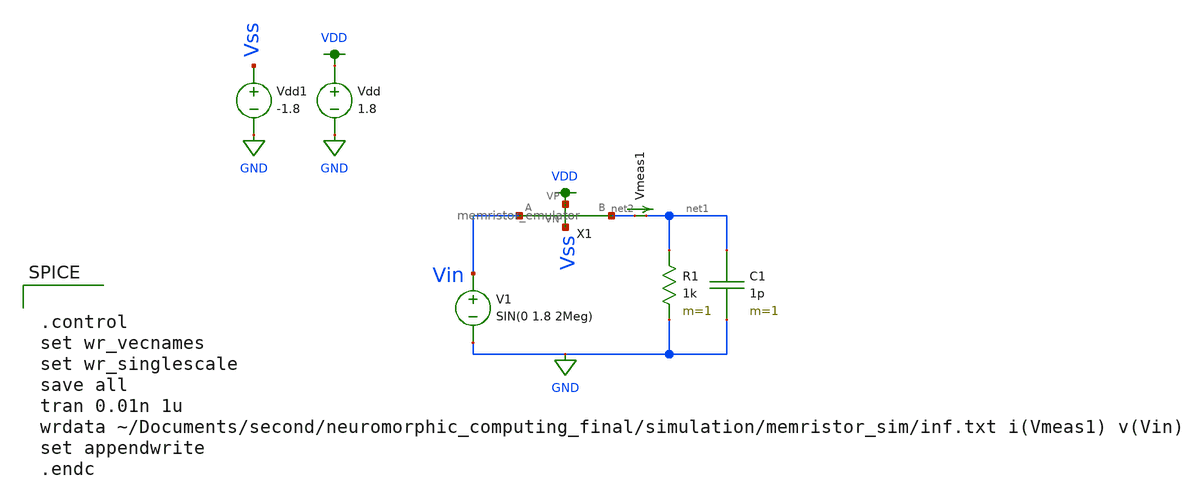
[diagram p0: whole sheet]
** sch_path: schematic/infinite.sch
**.subckt infinite
V1 Vin GND SIN(0 1.8 2Meg)
R1 net1 GND 1k m=1
C1 net1 GND 1p m=1
Vdd VDD GND 1.8
Vmeas1 net2 net1 0
.save i(vmeas1)
Vdd1 Vss GND -1.8
X1 VDD Vss net2 Vin memristor_emulator
**** begin user architecture code


.control
set wr_vecnames
set wr_singlescale
save all
tran 0.01n 1u
wrdata ~/Documents/second/neuromorphic_computing_final/simulation/memristor_sim/inf.txt i(Vmeas1)
+ v(Vin)
set appendwrite
.endc



.option wnflag=1
.param MC_SWITCH=1.0
.lib ~/skywater/skywater-pdk/libraries/sky130_fd_pr_ngspice/latest/models/sky130.lib.spice tt

**** end user architecture code
**.ends

* expanding   symbol:
*+  /home/madvlsi/Documents/second/neuromorphic_computing_final/schematic/memristor_emulator.sym # of pins=4
** sym_path: schematic/memristor_emulator.sym
** sch_path: schematic/memristor_emulator.sch
.subckt memristor_emulator VP VN B A
*.ipin A
*.iopin VN
*.iopin VP
*.opin B
XM1 B in_cap A B sky130_fd_pr__pfet_01v8 L=0.3 W=12 nf=1 ad='int((nf+1)/2) * W/nf * 0.29' as='int((nf+2)/2) * W/nf * 0.29'
+ pd='2*int((nf+1)/2) * (W/nf + 0.29)' ps='2*int((nf+2)/2) * (W/nf + 0.29)' nrd='0.29 / W' nrs='0.29 / W'
+ sa=0 sb=0 sd=0 mult=1 m=1
XM2 VP A in_cap VP sky130_fd_pr__pfet_01v8 L=2 W=3 nf=1 ad='int((nf+1)/2) * W/nf * 0.29' as='int((nf+2)/2) * W/nf * 0.29'
+ pd='2*int((nf+1)/2) * (W/nf + 0.29)' ps='2*int((nf+2)/2) * (W/nf + 0.29)' nrd='0.29 / W' nrs='0.29 / W'
+ sa=0 sb=0 sd=0 mult=1 m=1
XM3 VN in_cap VN VN sky130_fd_pr__nfet_01v8 L=20 W=20 nf=1 ad='int((nf+1)/2) * W/nf * 0.29' as='int((nf+2)/2) * W/nf * 0.29'
+ pd='2*int((nf+1)/2) * (W/nf + 0.29)' ps='2*int((nf+2)/2) * (W/nf + 0.29)' nrd='0.29 / W' nrs='0.29 / W'
+ sa=0 sb=0 sd=0 mult=1 m=1
XM4 VN B in_cap VN sky130_fd_pr__nfet_01v8 L=3 W=2 nf=1 ad='int((nf+1)/2) * W/nf * 0.29' as='int((nf+2)/2) * W/nf * 0.29'
+ pd='2*int((nf+1)/2) * (W/nf + 0.29)' ps='2*int((nf+2)/2) * (W/nf + 0.29)' nrd='0.29 / W' nrs='0.29 / W'
+ sa=0 sb=0 sd=0 mult=1 m=1
.ends

.GLOBAL VDD
.GLOBAL GND
.end
